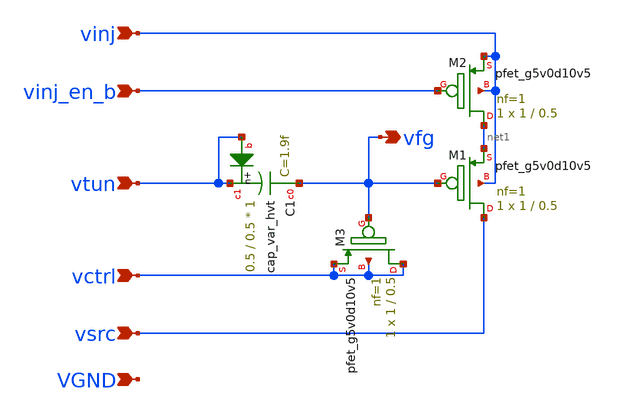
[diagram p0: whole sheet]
** sch_path: xschem/fgcell.sch
**.subckt fgcell vctrl vtun vinj vinj_en_b vsrc vfg VGND
*.ipin vctrl
*.ipin vtun
*.ipin vinj
*.ipin vinj_en_b
*.ipin vsrc
*.opin vfg
*.ipin VGND
XC1 vfg vtun vtun sky130_fd_pr__cap_var_hvt W=0.5 L=0.5 VM=1 m=1
XM1 vsrc vfg net1 vinj sky130_fd_pr__pfet_g5v0d10v5 L=0.5 W=1 nf=1 ad='int((nf+1)/2) * W/nf * 0.29' as='int((nf+2)/2) * W/nf * 0.29'
+ pd='2*int((nf+1)/2) * (W/nf + 0.29)' ps='2*int((nf+2)/2) * (W/nf + 0.29)' nrd='0.29 / W' nrs='0.29 / W'
+ sa=0 sb=0 sd=0 mult=1 m=1
XM2 net1 vinj_en_b vinj vinj sky130_fd_pr__pfet_g5v0d10v5 L=0.5 W=1 nf=1 ad='int((nf+1)/2) * W/nf * 0.29'
+ as='int((nf+2)/2) * W/nf * 0.29' pd='2*int((nf+1)/2) * (W/nf + 0.29)' ps='2*int((nf+2)/2) * (W/nf + 0.29)'
+ nrd='0.29 / W' nrs='0.29 / W' sa=0 sb=0 sd=0 mult=1 m=1
XM3 vctrl vfg vctrl vctrl sky130_fd_pr__pfet_g5v0d10v5 L=0.5 W=1 nf=1 ad='int((nf+1)/2) * W/nf * 0.29'
+ as='int((nf+2)/2) * W/nf * 0.29' pd='2*int((nf+1)/2) * (W/nf + 0.29)' ps='2*int((nf+2)/2) * (W/nf + 0.29)'
+ nrd='0.29 / W' nrs='0.29 / W' sa=0 sb=0 sd=0 mult=1 m=1
**.ends
.end
